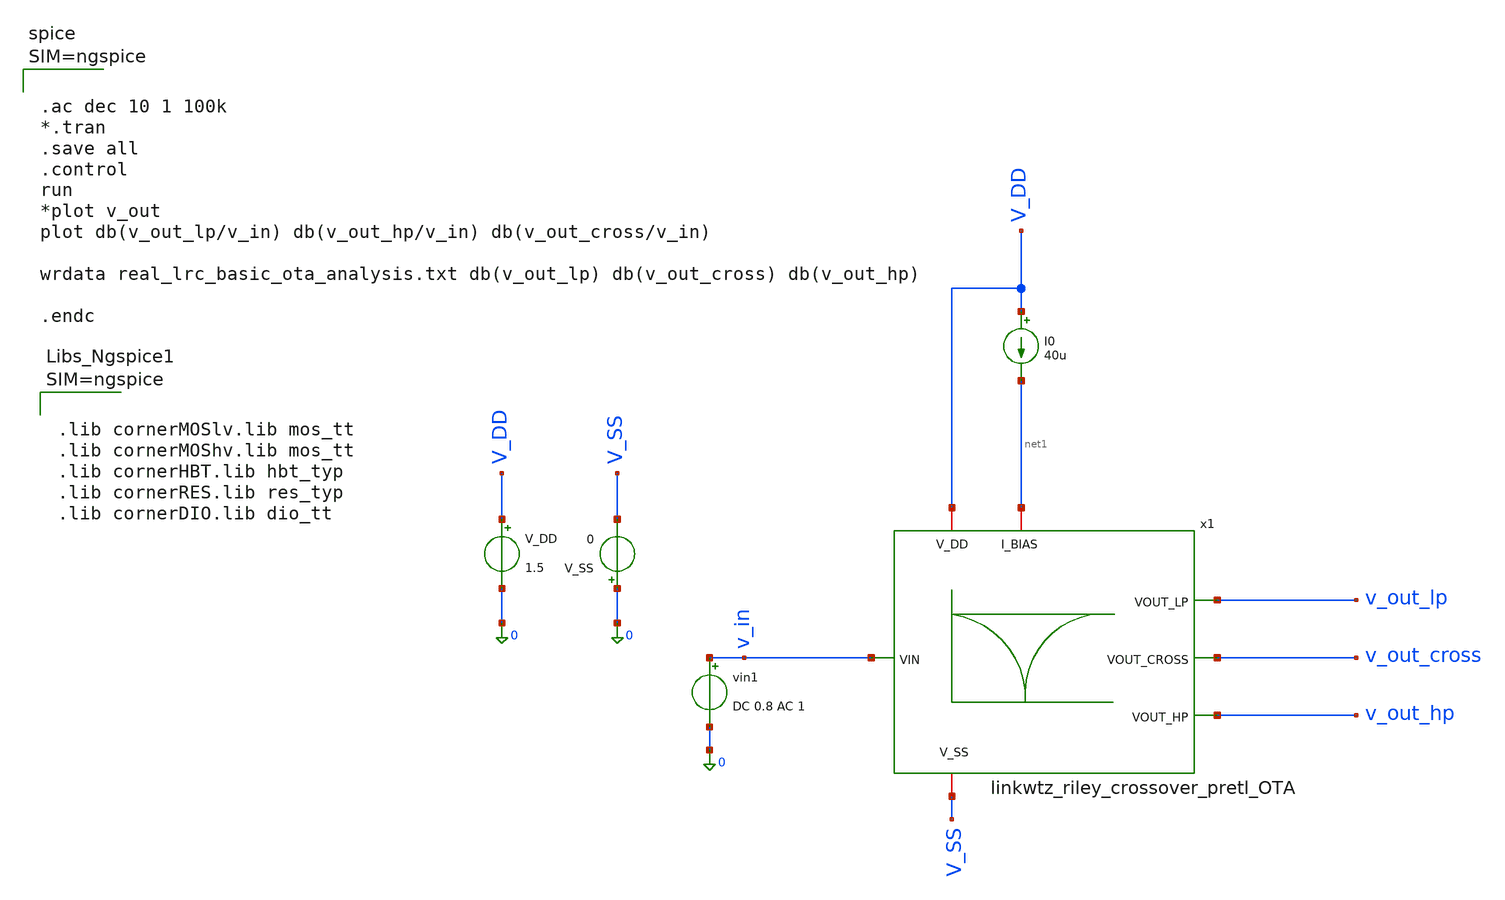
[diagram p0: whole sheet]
** sch_path: 004_Real_Circuits/001_version_basic_ota_pretl/linkwitz_riley_real_circuit_pretl_top_tb.sch
**.subckt linkwitz_riley_real_circuit_pretl_top_tb
I0 V_DD net1 40u
vin1 v_in 0 DC 0.8 AC 1
x1 v_out_lp net1 V_DD v_out_cross V_SS v_in v_out_hp linkwtz_riley_crossover_pretl_OTA
V_DD V_DD 0 1.5
V_SS 0 V_SS 0
**** begin user architecture code



.lib cornerMOSlv.lib mos_tt
.lib cornerMOShv.lib mos_tt
.lib cornerHBT.lib hbt_typ
.lib cornerRES.lib res_typ
.lib cornerDIO.lib dio_tt






.ac dec 10 1 100k
*.tran
.save all
.control
run
*plot v_out
plot db(v_out_lp/v_in) db(v_out_hp/v_in) db(v_out_cross/v_in)

wrdata real_lrc_basic_ota_analysis.txt db(v_out_lp) db(v_out_cross) db(v_out_hp)

.endc



**** end user architecture code
**.ends
.end
